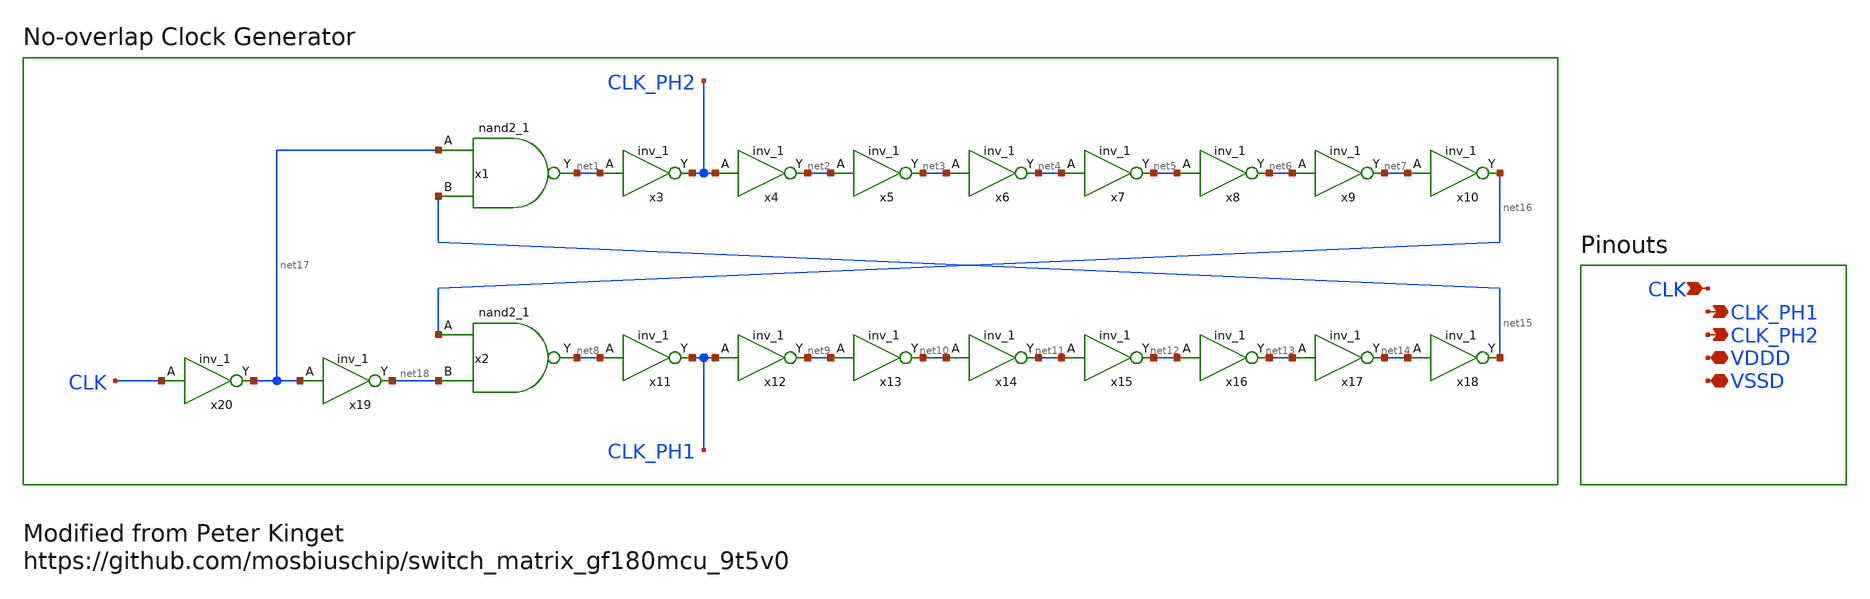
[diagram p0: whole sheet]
** sch_path: designs/libs/core_switch_matrix/nooverlap_generator/nooverlap_generator.sch
**.subckt nooverlap_generator CLK CLK_PH1 VDDD VSSD CLK_PH2
*.ipin CLK
*.opin CLK_PH1
*.iopin VDDD
*.iopin VSSD
*.opin CLK_PH2
x1 net17 net15 VSSD VDDD VSSD VDDD net1 gf180mcu_fd_sc_mcu9t5v0__nand2_1
x2 net16 net18 VSSD VDDD VSSD VDDD net8 gf180mcu_fd_sc_mcu9t5v0__nand2_1
x3 net1 VSSD VDDD VSSD VDDD CLK_PH2 gf180mcu_fd_sc_mcu9t5v0__inv_1
x4 CLK_PH2 VSSD VDDD VSSD VDDD net2 gf180mcu_fd_sc_mcu9t5v0__inv_1
x5 net2 VSSD VDDD VSSD VDDD net3 gf180mcu_fd_sc_mcu9t5v0__inv_1
x6 net3 VSSD VDDD VSSD VDDD net4 gf180mcu_fd_sc_mcu9t5v0__inv_1
x7 net4 VSSD VDDD VSSD VDDD net5 gf180mcu_fd_sc_mcu9t5v0__inv_1
x8 net5 VSSD VDDD VSSD VDDD net6 gf180mcu_fd_sc_mcu9t5v0__inv_1
x9 net6 VSSD VDDD VSSD VDDD net7 gf180mcu_fd_sc_mcu9t5v0__inv_1
x10 net7 VSSD VDDD VSSD VDDD net16 gf180mcu_fd_sc_mcu9t5v0__inv_1
x11 net8 VSSD VDDD VSSD VDDD CLK_PH1 gf180mcu_fd_sc_mcu9t5v0__inv_1
x12 CLK_PH1 VSSD VDDD VSSD VDDD net9 gf180mcu_fd_sc_mcu9t5v0__inv_1
x13 net9 VSSD VDDD VSSD VDDD net10 gf180mcu_fd_sc_mcu9t5v0__inv_1
x14 net10 VSSD VDDD VSSD VDDD net11 gf180mcu_fd_sc_mcu9t5v0__inv_1
x15 net11 VSSD VDDD VSSD VDDD net12 gf180mcu_fd_sc_mcu9t5v0__inv_1
x16 net12 VSSD VDDD VSSD VDDD net13 gf180mcu_fd_sc_mcu9t5v0__inv_1
x17 net13 VSSD VDDD VSSD VDDD net14 gf180mcu_fd_sc_mcu9t5v0__inv_1
x18 net14 VSSD VDDD VSSD VDDD net15 gf180mcu_fd_sc_mcu9t5v0__inv_1
x19 net17 VSSD VDDD VSSD VDDD net18 gf180mcu_fd_sc_mcu9t5v0__inv_1
x20 CLK VSSD VDDD VSSD VDDD net17 gf180mcu_fd_sc_mcu9t5v0__inv_1
**.ends
.end
